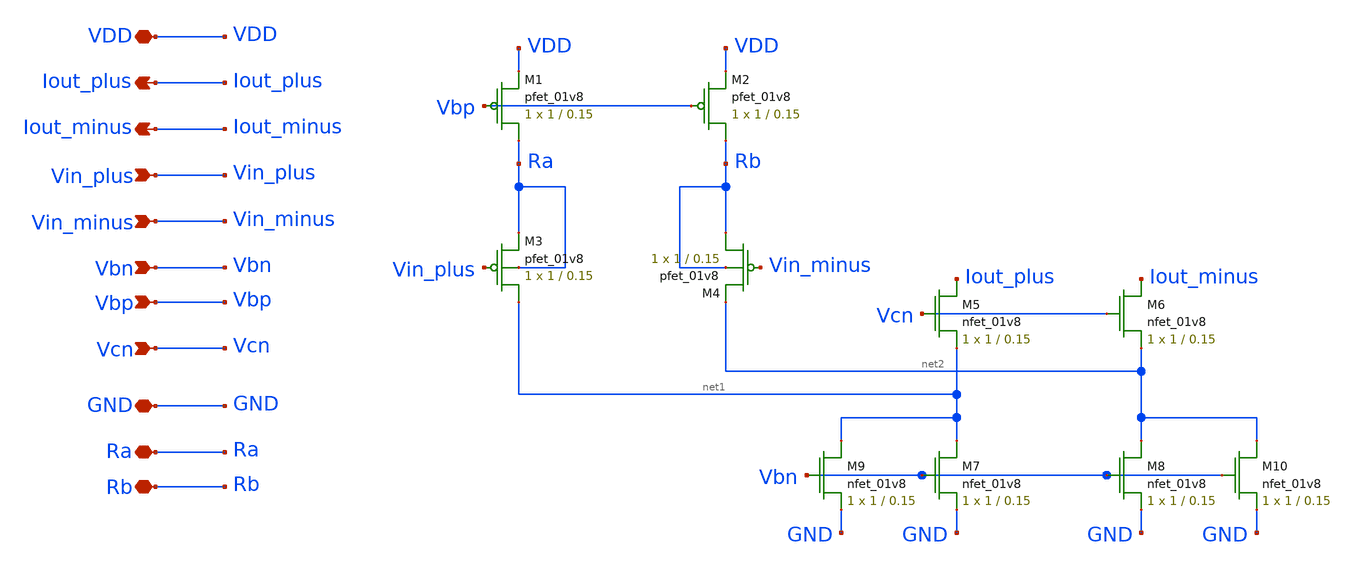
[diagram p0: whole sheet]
** sch_path: final/schematics/brad_VI_input.sch
**.subckt brad_VI_input Iout_plus Iout_minus VDD Vin_plus Vin_minus Vbn GND Ra Rb Vbp Vcn
*.opin Iout_plus
*.opin Iout_minus
*.iopin VDD
*.ipin Vin_plus
*.ipin Vin_minus
*.ipin Vbn
*.iopin GND
*.iopin Ra
*.iopin Rb
*.ipin Vbp
*.ipin Vcn
XM1 Ra Vbp VDD VDD sky130_fd_pr__pfet_01v8 L=0.15 W=1 nf=1 ad='int((nf+1)/2) * W/nf * 0.29' as='int((nf+2)/2) * W/nf * 0.29'
+ pd='2*int((nf+1)/2) * (W/nf + 0.29)' ps='2*int((nf+2)/2) * (W/nf + 0.29)' nrd='0.29 / W' nrs='0.29 / W'
+ sa=0 sb=0 sd=0 mult=1 m=1
XM2 Rb Vbp VDD VDD sky130_fd_pr__pfet_01v8 L=0.15 W=1 nf=1 ad='int((nf+1)/2) * W/nf * 0.29' as='int((nf+2)/2) * W/nf * 0.29'
+ pd='2*int((nf+1)/2) * (W/nf + 0.29)' ps='2*int((nf+2)/2) * (W/nf + 0.29)' nrd='0.29 / W' nrs='0.29 / W'
+ sa=0 sb=0 sd=0 mult=1 m=1
XM3 net1 Vin_plus Ra Ra sky130_fd_pr__pfet_01v8 L=0.15 W=1 nf=1 ad='int((nf+1)/2) * W/nf * 0.29' as='int((nf+2)/2) * W/nf * 0.29'
+ pd='2*int((nf+1)/2) * (W/nf + 0.29)' ps='2*int((nf+2)/2) * (W/nf + 0.29)' nrd='0.29 / W' nrs='0.29 / W'
+ sa=0 sb=0 sd=0 mult=1 m=1
XM4 Rb Vin_minus net2 Rb sky130_fd_pr__pfet_01v8 L=0.15 W=1 nf=1 ad='int((nf+1)/2) * W/nf * 0.29' as='int((nf+2)/2) * W/nf * 0.29'
+ pd='2*int((nf+1)/2) * (W/nf + 0.29)' ps='2*int((nf+2)/2) * (W/nf + 0.29)' nrd='0.29 / W' nrs='0.29 / W'
+ sa=0 sb=0 sd=0 mult=1 m=1
XM5 Iout_plus Vcn net1 GND sky130_fd_pr__nfet_01v8 L=0.15 W=1 nf=1 ad='int((nf+1)/2) * W/nf * 0.29' as='int((nf+2)/2) * W/nf * 0.29'
+ pd='2*int((nf+1)/2) * (W/nf + 0.29)' ps='2*int((nf+2)/2) * (W/nf + 0.29)' nrd='0.29 / W' nrs='0.29 / W'
+ sa=0 sb=0 sd=0 mult=1 m=1
XM6 Iout_minus Vcn net2 GND sky130_fd_pr__nfet_01v8 L=0.15 W=1 nf=1 ad='int((nf+1)/2) * W/nf * 0.29'
+ as='int((nf+2)/2) * W/nf * 0.29' pd='2*int((nf+1)/2) * (W/nf + 0.29)' ps='2*int((nf+2)/2) * (W/nf + 0.29)'
+ nrd='0.29 / W' nrs='0.29 / W' sa=0 sb=0 sd=0 mult=1 m=1
XM7 net1 Vbn GND GND sky130_fd_pr__nfet_01v8 L=0.15 W=1 nf=1 ad='int((nf+1)/2) * W/nf * 0.29' as='int((nf+2)/2) * W/nf * 0.29'
+ pd='2*int((nf+1)/2) * (W/nf + 0.29)' ps='2*int((nf+2)/2) * (W/nf + 0.29)' nrd='0.29 / W' nrs='0.29 / W'
+ sa=0 sb=0 sd=0 mult=1 m=1
XM8 net2 Vbn GND GND sky130_fd_pr__nfet_01v8 L=0.15 W=1 nf=1 ad='int((nf+1)/2) * W/nf * 0.29' as='int((nf+2)/2) * W/nf * 0.29'
+ pd='2*int((nf+1)/2) * (W/nf + 0.29)' ps='2*int((nf+2)/2) * (W/nf + 0.29)' nrd='0.29 / W' nrs='0.29 / W'
+ sa=0 sb=0 sd=0 mult=1 m=1
XM9 net1 Vbn GND GND sky130_fd_pr__nfet_01v8 L=0.15 W=1 nf=1 ad='int((nf+1)/2) * W/nf * 0.29' as='int((nf+2)/2) * W/nf * 0.29'
+ pd='2*int((nf+1)/2) * (W/nf + 0.29)' ps='2*int((nf+2)/2) * (W/nf + 0.29)' nrd='0.29 / W' nrs='0.29 / W'
+ sa=0 sb=0 sd=0 mult=1 m=1
XM10 net2 Vbn GND GND sky130_fd_pr__nfet_01v8 L=0.15 W=1 nf=1 ad='int((nf+1)/2) * W/nf * 0.29' as='int((nf+2)/2) * W/nf * 0.29'
+ pd='2*int((nf+1)/2) * (W/nf + 0.29)' ps='2*int((nf+2)/2) * (W/nf + 0.29)' nrd='0.29 / W' nrs='0.29 / W'
+ sa=0 sb=0 sd=0 mult=1 m=1
**.ends
.end
